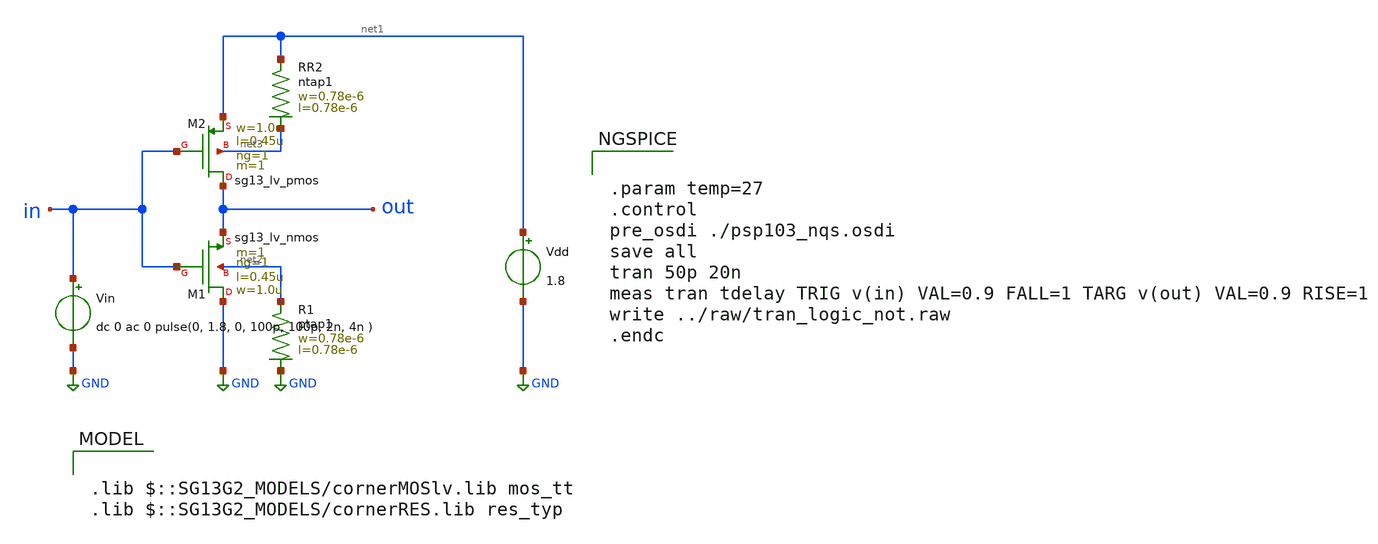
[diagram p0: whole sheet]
** sch_path: ihp-sg13g2/libs.tech/xschem/sg13g2_tests/tran_logic_not.sch
* Copyright 2023 IHP PDK Authors
**.subckt tran_logic_not
Vin in GND dc 0 ac 0 pulse(0, 1.8, 0, 100p, 100p, 2n, 4n )
Vdd net1 GND 1.8
XM1 GND in out net2 sg13_lv_nmos w=1.0u l=0.45u ng=1 m=1 mm_ok=1
XR1 net2 GND ptap1 R=262.8 w=0.78e-6 l=0.78e-6
XR2 net1 net3 ntap1 R=262.8 w=0.78e-6 l=0.78e-6
XM2 out in net1 net3 sg13_lv_pmos w=1.0u l=0.45u ng=1 m=1 mm_ok=1
**** begin user architecture code

.lib $::SG13G2_MODELS/cornerMOSlv.lib mos_tt
.lib $::SG13G2_MODELS/cornerRES.lib res_typ



.param temp=27
.control
pre_osdi ./psp103_nqs.osdi
save all
tran 50p 20n
meas tran tdelay TRIG v(in) VAL=0.9 FALL=1 TARG v(out) VAL=0.9 RISE=1
write ../raw/tran_logic_not.raw
.endc


**** end user architecture code
**.ends
.GLOBAL GND
.end
